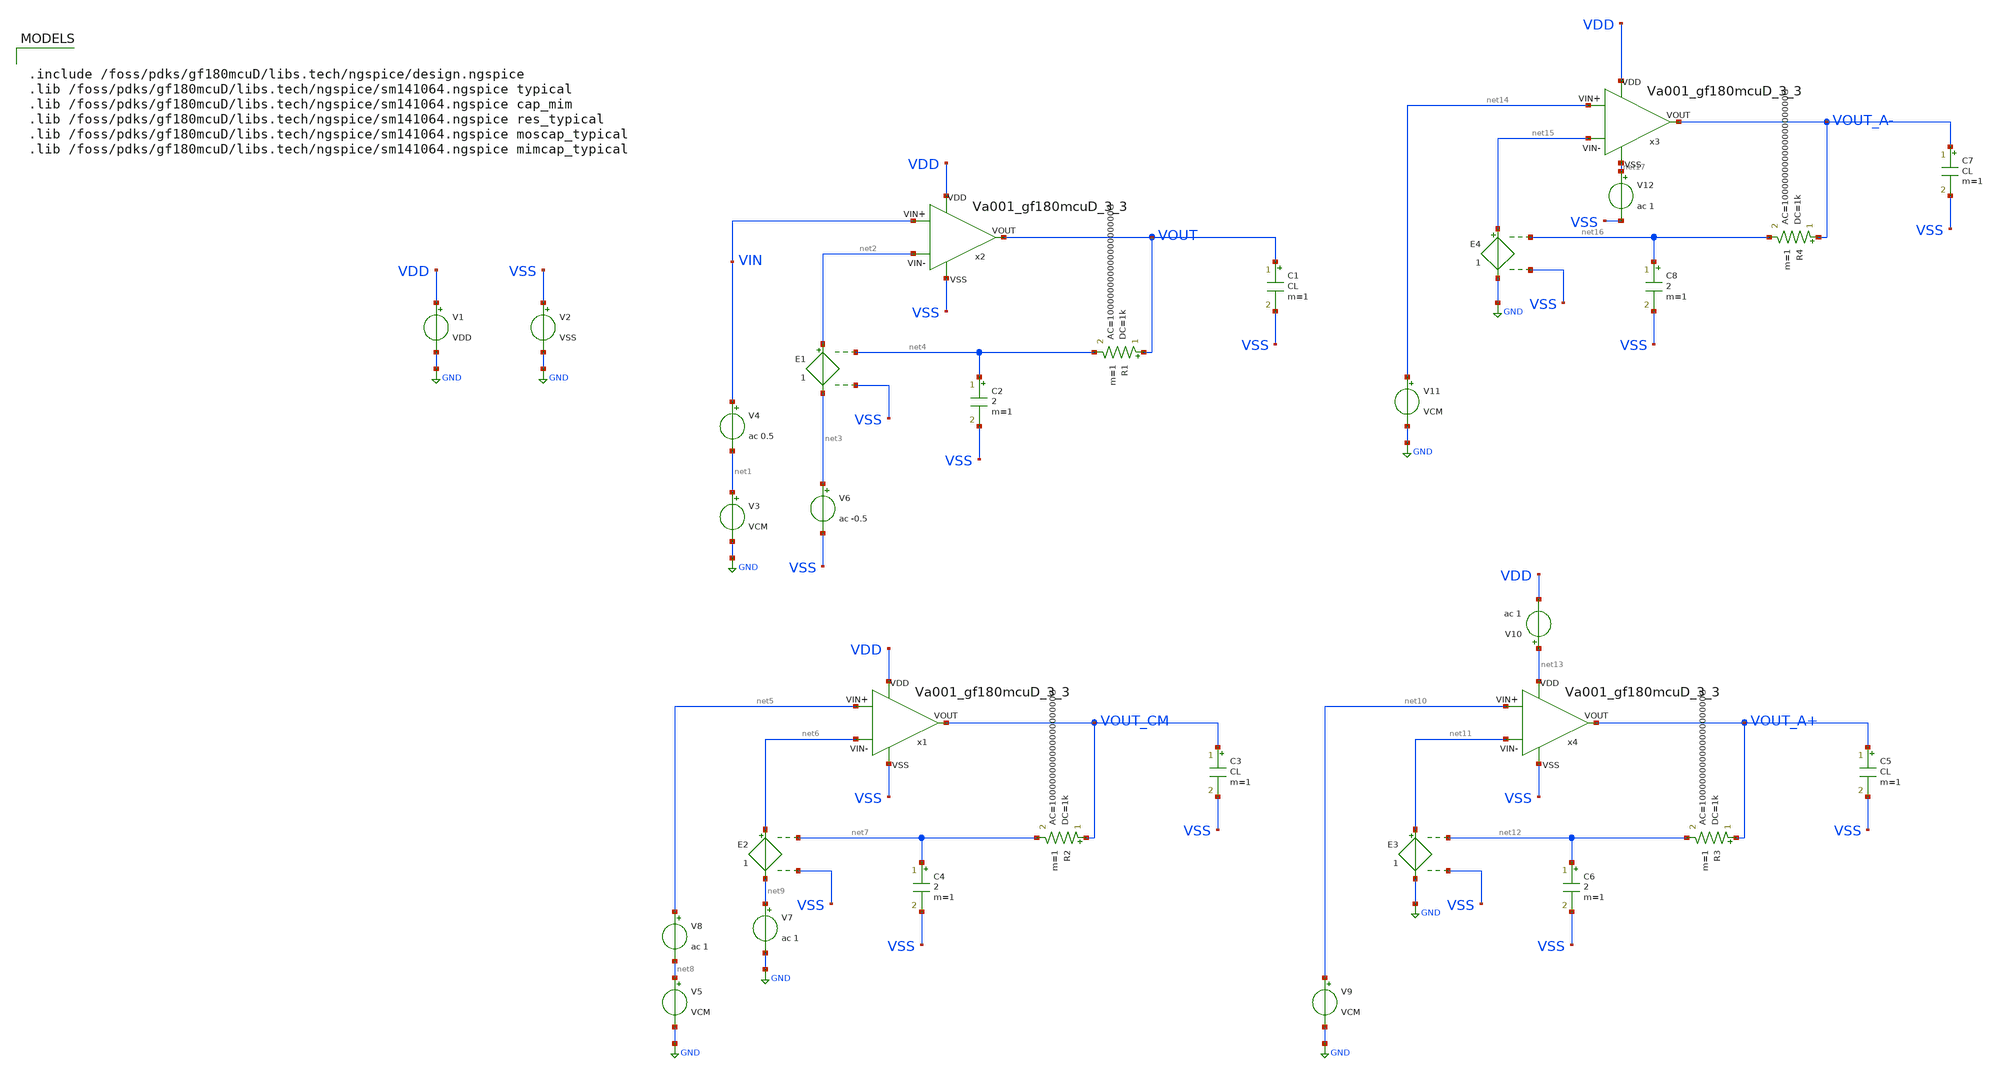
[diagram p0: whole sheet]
** sch_path: Learning/single_ended_amplifiers/VA001_series/Design_and_Analysis_of_Two-Stage_CMOS_Operational_Amplifier_for_Fluorescence_Signal_Processing_gf180mcu_3_3V/amplifier_design/full.sch
**.subckt full
V1 VDD GND VDD
V2 VSS GND VSS
V3 net1 GND VCM
V4 VIN net1 ac 0.5
V6 net3 VSS ac -0.5
C1 VOUT VSS CL m=1
R1 VOUT net4 1k ac=10000000000000000000G m=1
C2 net4 VSS 2 m=1
E1 net2 net3 net4 VSS 1
V5 net8 GND VCM
V8 net5 net8 ac 1
C3 VOUT_CM VSS CL m=1
R2 VOUT_CM net7 1k ac=10000000000000000000G m=1
C4 net7 VSS 2 m=1
E2 net6 net9 net7 VSS 1
V7 net9 GND ac 1
V9 net10 GND VCM
V10 net13 VDD ac 1
C5 VOUT_A+ VSS CL m=1
R3 VOUT_A+ net12 1k ac=10000000000000000000G m=1
C6 net12 VSS 2 m=1
E3 net11 GND net12 VSS 1
V11 net14 GND VCM
V12 net17 VSS ac 1
C7 VOUT_A- VSS CL m=1
R4 VOUT_A- net16 1k ac=10000000000000000000G m=1
C8 net16 VSS 2 m=1
E4 net15 GND net16 VSS 1
x1 VDD VSS net6 net5 VOUT_CM Va001_gf180mcuD_3_3
x2 VDD VSS net2 VIN VOUT Va001_gf180mcuD_3_3
x3 VDD net17 net15 net14 VOUT_A- Va001_gf180mcuD_3_3
x4 net13 VSS net11 net10 VOUT_A+ Va001_gf180mcuD_3_3
**** begin user architecture code

.include /foss/pdks/gf180mcuD/libs.tech/ngspice/design.ngspice
.lib /foss/pdks/gf180mcuD/libs.tech/ngspice/sm141064.ngspice typical
.lib /foss/pdks/gf180mcuD/libs.tech/ngspice/sm141064.ngspice cap_mim
.lib /foss/pdks/gf180mcuD/libs.tech/ngspice/sm141064.ngspice res_typical
.lib /foss/pdks/gf180mcuD/libs.tech/ngspice/sm141064.ngspice moscap_typical
.lib /foss/pdks/gf180mcuD/libs.tech/ngspice/sm141064.ngspice mimcap_typical

**** end user architecture code
**.ends
.GLOBAL GND
**** begin user architecture code


.param VDD = 3.3
.param VSS = 0
.param VCM = 1.65
.param V_OFF =-386u
.param CL =3p


.param mm_ok=0
.param mc_ok=0

.param temp=27
.control
save all
ac dec 1000 1 10G
plot db(v(VOUT)) (180+(180*ph(v(VOUT))/pi))
plot (db(v(VOUT)) - db(v(VOUT_CM)))
plot (db(v(VOUT)) - db(v(VOUT_A-)))
plot (db(v(VOUT))- db(v(VOUT_A+)))

op
print (-3.3*i(Vmeas))
print (1.65-v(VOUT))

.endc


**** end user architecture code
.end
